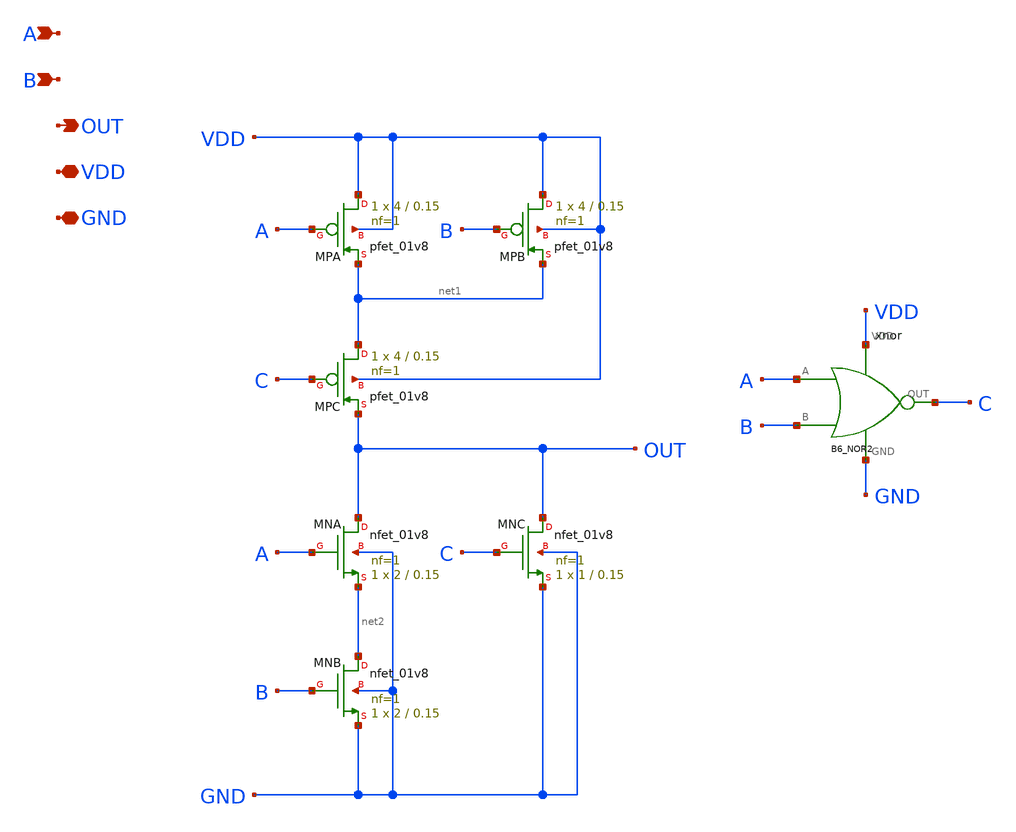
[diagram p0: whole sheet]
** sch_path: blocks/06_Clock_gen/xschem/B6_XOR.sch
**.subckt B6_XOR A B OUT VDD GND
*.ipin A
*.ipin B
*.opin OUT
*.iopin VDD
*.iopin GND
XMPA VDD A net1 VDD sky130_fd_pr__pfet_01v8 L=0.15 W=4 nf=1 ad='int((1 + 1)/2) * 4 / 1 * 0.29' as='int((1 + 2)/2) * 4 / 1 * 0.29'
+ pd='2*int((1 + 1)/2) * (4 / 1 + 0.29)' ps='2*int((1 + 2)/2) * (4 / 1 + 0.29)' nrd='0.29 / 4 ' nrs='0.29 / 4 '
+ sa=0 sb=0 sd=0 mult=1 m=1
XMPB VDD B net1 VDD sky130_fd_pr__pfet_01v8 L=0.15 W=4 nf=1 ad='int((1 + 1)/2) * 4 / 1 * 0.29' as='int((1 + 2)/2) * 4 / 1 * 0.29'
+ pd='2*int((1 + 1)/2) * (4 / 1 + 0.29)' ps='2*int((1 + 2)/2) * (4 / 1 + 0.29)' nrd='0.29 / 4 ' nrs='0.29 / 4 '
+ sa=0 sb=0 sd=0 mult=1 m=1
XMPC net1 C OUT VDD sky130_fd_pr__pfet_01v8 L=0.15 W=4 nf=1 ad='int((1 + 1)/2) * 4 / 1 * 0.29' as='int((1 + 2)/2) * 4 / 1 * 0.29'
+ pd='2*int((1 + 1)/2) * (4 / 1 + 0.29)' ps='2*int((1 + 2)/2) * (4 / 1 + 0.29)' nrd='0.29 / 4 ' nrs='0.29 / 4 '
+ sa=0 sb=0 sd=0 mult=1 m=1
XMNA OUT A net2 GND sky130_fd_pr__nfet_01v8 L=0.15 W=2 nf=1 ad='int((1 + 1)/2) * 2 / 1 * 0.29' as='int((1 + 2)/2) * 2 / 1 * 0.29'
+ pd='2*int((1 + 1)/2) * (2 / 1 + 0.29)' ps='2*int((1 + 2)/2) * (2 / 1 + 0.29)' nrd='0.29 / 2 ' nrs='0.29 / 2 '
+ sa=0 sb=0 sd=0 mult=1 m=1
XMNB net2 B GND GND sky130_fd_pr__nfet_01v8 L=0.15 W=2 nf=1 ad='int((1 + 1)/2) * 2 / 1 * 0.29' as='int((1 + 2)/2) * 2 / 1 * 0.29'
+ pd='2*int((1 + 1)/2) * (2 / 1 + 0.29)' ps='2*int((1 + 2)/2) * (2 / 1 + 0.29)' nrd='0.29 / 2 ' nrs='0.29 / 2 '
+ sa=0 sb=0 sd=0 mult=1 m=1
XMNC OUT C GND GND sky130_fd_pr__nfet_01v8 L=0.15 W=1 nf=1 ad='int((1 + 1)/2) * 1 / 1 * 0.29' as='int((1 + 2)/2) * 1 / 1 * 0.29'
+ pd='2*int((1 + 1)/2) * (1 / 1 + 0.29)' ps='2*int((1 + 2)/2) * (1 / 1 + 0.29)' nrd='0.29 / 1 ' nrs='0.29 / 1 '
+ sa=0 sb=0 sd=0 mult=1 m=1
xnor A B C VDD GND B6_NOR2
**.ends

* expanding   symbol:  blocks/06_Clock_gen/xschem/B6_NOR2.sym # of pins=5
** sym_path: blocks/06_Clock_gen/xschem/B6_NOR2.sym
** sch_path: blocks/06_Clock_gen/xschem/B6_NOR2.sch
.subckt B6_NOR2 A B OUT VDD GND
*.ipin A
*.ipin B
*.opin OUT
*.iopin VDD
*.iopin GND
XMPA VDD A net1 VDD sky130_fd_pr__pfet_01v8 L=0.15 W=4 nf=1 ad='int((1 + 1)/2) * 4 / 1 * 0.29' as='int((1 + 2)/2) * 4 / 1 * 0.29'
+ pd='2*int((1 + 1)/2) * (4 / 1 + 0.29)' ps='2*int((1 + 2)/2) * (4 / 1 + 0.29)' nrd='0.29 / 4 ' nrs='0.29 / 4 '
+ sa=0 sb=0 sd=0 mult=1 m=1
XMPB net1 B OUT VDD sky130_fd_pr__pfet_01v8 L=0.15 W=4 nf=1 ad='int((1 + 1)/2) * 4 / 1 * 0.29' as='int((1 + 2)/2) * 4 / 1 * 0.29'
+ pd='2*int((1 + 1)/2) * (4 / 1 + 0.29)' ps='2*int((1 + 2)/2) * (4 / 1 + 0.29)' nrd='0.29 / 4 ' nrs='0.29 / 4 '
+ sa=0 sb=0 sd=0 mult=1 m=1
XMNA OUT A GND GND sky130_fd_pr__nfet_01v8 L=0.15 W=1 nf=1 ad='int((1 + 1)/2) * 1 / 1 * 0.29' as='int((1 + 2)/2) * 1 / 1 * 0.29'
+ pd='2*int((1 + 1)/2) * (1 / 1 + 0.29)' ps='2*int((1 + 2)/2) * (1 / 1 + 0.29)' nrd='0.29 / 1 ' nrs='0.29 / 1 '
+ sa=0 sb=0 sd=0 mult=1 m=1
XMNB OUT B GND GND sky130_fd_pr__nfet_01v8 L=0.15 W=1 nf=1 ad='int((1 + 1)/2) * 1 / 1 * 0.29' as='int((1 + 2)/2) * 1 / 1 * 0.29'
+ pd='2*int((1 + 1)/2) * (1 / 1 + 0.29)' ps='2*int((1 + 2)/2) * (1 / 1 + 0.29)' nrd='0.29 / 1 ' nrs='0.29 / 1 '
+ sa=0 sb=0 sd=0 mult=1 m=1
.ends

.end
